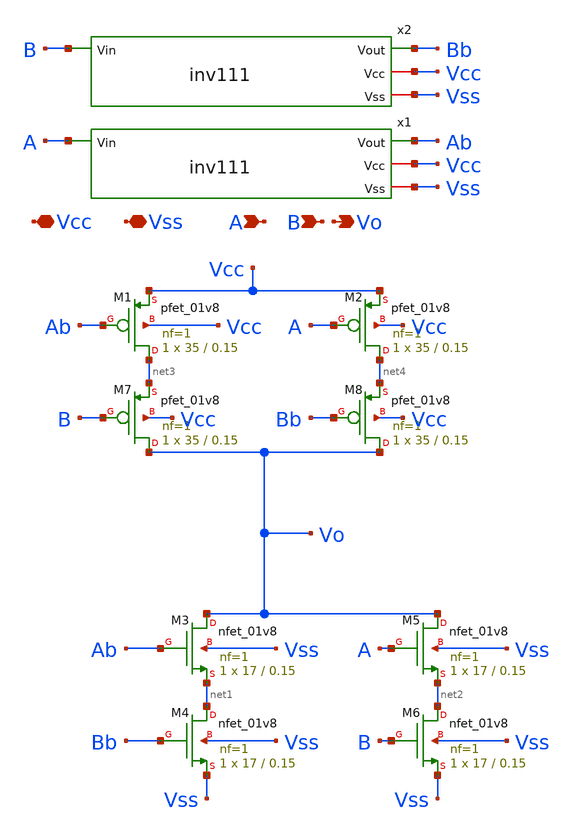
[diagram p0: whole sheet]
** sch_path: Git Files/Simulation Schematic/Pre Emphasis Driver/xor.sch
**.subckt xor Vcc Vss A Vo B
*.iopin Vcc
*.iopin Vss
*.ipin A
*.opin Vo
*.ipin B
XM1 net3 Ab Vcc Vcc sky130_fd_pr__pfet_01v8 L=0.15 W=35 nf=1 ad='int((nf+1)/2) * W/nf * 0.29' as='int((nf+2)/2) * W/nf * 0.29'
+ pd='2*int((nf+1)/2) * (W/nf + 0.29)' ps='2*int((nf+2)/2) * (W/nf + 0.29)' nrd='0.29 / W' nrs='0.29 / W'
+ sa=0 sb=0 sd=0 mult=1 m=1
XM2 net4 A Vcc Vcc sky130_fd_pr__pfet_01v8 L=0.15 W=35 nf=1 ad='int((nf+1)/2) * W/nf * 0.29' as='int((nf+2)/2) * W/nf * 0.29'
+ pd='2*int((nf+1)/2) * (W/nf + 0.29)' ps='2*int((nf+2)/2) * (W/nf + 0.29)' nrd='0.29 / W' nrs='0.29 / W'
+ sa=0 sb=0 sd=0 mult=1 m=1
XM3 Vo Ab net1 Vss sky130_fd_pr__nfet_01v8 L=0.15 W=17 nf=1 ad='int((nf+1)/2) * W/nf * 0.29' as='int((nf+2)/2) * W/nf * 0.29'
+ pd='2*int((nf+1)/2) * (W/nf + 0.29)' ps='2*int((nf+2)/2) * (W/nf + 0.29)' nrd='0.29 / W' nrs='0.29 / W'
+ sa=0 sb=0 sd=0 mult=1 m=1
XM4 net1 Bb Vss Vss sky130_fd_pr__nfet_01v8 L=0.15 W=17 nf=1 ad='int((nf+1)/2) * W/nf * 0.29' as='int((nf+2)/2) * W/nf * 0.29'
+ pd='2*int((nf+1)/2) * (W/nf + 0.29)' ps='2*int((nf+2)/2) * (W/nf + 0.29)' nrd='0.29 / W' nrs='0.29 / W'
+ sa=0 sb=0 sd=0 mult=1 m=1
XM5 Vo A net2 Vss sky130_fd_pr__nfet_01v8 L=0.15 W=17 nf=1 ad='int((nf+1)/2) * W/nf * 0.29' as='int((nf+2)/2) * W/nf * 0.29'
+ pd='2*int((nf+1)/2) * (W/nf + 0.29)' ps='2*int((nf+2)/2) * (W/nf + 0.29)' nrd='0.29 / W' nrs='0.29 / W'
+ sa=0 sb=0 sd=0 mult=1 m=1
XM6 net2 B Vss Vss sky130_fd_pr__nfet_01v8 L=0.15 W=17 nf=1 ad='int((nf+1)/2) * W/nf * 0.29' as='int((nf+2)/2) * W/nf * 0.29'
+ pd='2*int((nf+1)/2) * (W/nf + 0.29)' ps='2*int((nf+2)/2) * (W/nf + 0.29)' nrd='0.29 / W' nrs='0.29 / W'
+ sa=0 sb=0 sd=0 mult=1 m=1
x1 A Ab Vcc Vss inv111
x2 B Bb Vcc Vss inv111
XM7 Vo B net3 Vcc sky130_fd_pr__pfet_01v8 L=0.15 W=35 nf=1 ad='int((nf+1)/2) * W/nf * 0.29' as='int((nf+2)/2) * W/nf * 0.29'
+ pd='2*int((nf+1)/2) * (W/nf + 0.29)' ps='2*int((nf+2)/2) * (W/nf + 0.29)' nrd='0.29 / W' nrs='0.29 / W'
+ sa=0 sb=0 sd=0 mult=1 m=1
XM8 Vo Bb net4 Vcc sky130_fd_pr__pfet_01v8 L=0.15 W=35 nf=1 ad='int((nf+1)/2) * W/nf * 0.29' as='int((nf+2)/2) * W/nf * 0.29'
+ pd='2*int((nf+1)/2) * (W/nf + 0.29)' ps='2*int((nf+2)/2) * (W/nf + 0.29)' nrd='0.29 / W' nrs='0.29 / W'
+ sa=0 sb=0 sd=0 mult=1 m=1
**.ends
.end
